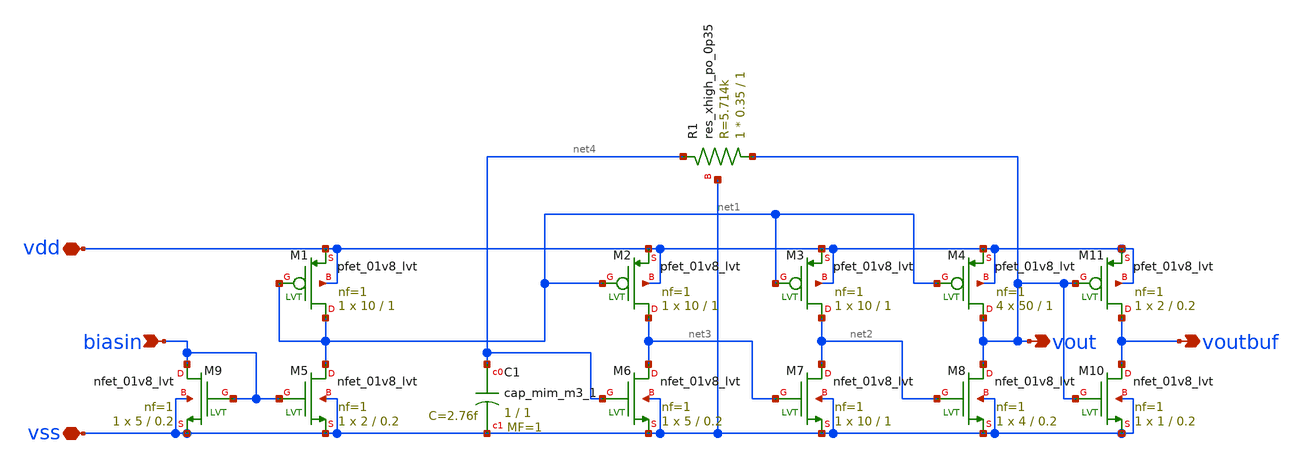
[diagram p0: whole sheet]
** sch_path: Circuits/lowpowersystem1/xschem/lphysteresistoscillatorsym5.sch
**.subckt lphysteresistoscillatorsym5 biasin vss vdd voutbuf vout
*.ipin biasin
*.iopin vss
*.iopin vdd
*.opin voutbuf
*.opin vout
XM1 net1 net1 vdd vdd sky130_fd_pr__pfet_01v8_lvt L=1 W=10 nf=1 ad='int((nf+1)/2) * W/nf * 0.29' as='int((nf+2)/2) * W/nf * 0.29'
+ pd='2*int((nf+1)/2) * (W/nf + 0.29)' ps='2*int((nf+2)/2) * (W/nf + 0.29)' nrd='0.29 / W' nrs='0.29 / W'
+ sa=0 sb=0 sd=0 mult=1 m=1
XM2 net3 net1 vdd vdd sky130_fd_pr__pfet_01v8_lvt L=1 W=10 nf=1 ad='int((nf+1)/2) * W/nf * 0.29' as='int((nf+2)/2) * W/nf * 0.29'
+ pd='2*int((nf+1)/2) * (W/nf + 0.29)' ps='2*int((nf+2)/2) * (W/nf + 0.29)' nrd='0.29 / W' nrs='0.29 / W'
+ sa=0 sb=0 sd=0 mult=1 m=1
XM3 net2 net1 vdd vdd sky130_fd_pr__pfet_01v8_lvt L=1 W=10 nf=1 ad='int((nf+1)/2) * W/nf * 0.29' as='int((nf+2)/2) * W/nf * 0.29'
+ pd='2*int((nf+1)/2) * (W/nf + 0.29)' ps='2*int((nf+2)/2) * (W/nf + 0.29)' nrd='0.29 / W' nrs='0.29 / W'
+ sa=0 sb=0 sd=0 mult=1 m=1
XM4 vout net1 vdd vdd sky130_fd_pr__pfet_01v8_lvt L=1 W=50 nf=1 ad='int((nf+1)/2) * W/nf * 0.29' as='int((nf+2)/2) * W/nf * 0.29'
+ pd='2*int((nf+1)/2) * (W/nf + 0.29)' ps='2*int((nf+2)/2) * (W/nf + 0.29)' nrd='0.29 / W' nrs='0.29 / W'
+ sa=0 sb=0 sd=0 mult=4 m=4
XM5 net1 biasin vss vss sky130_fd_pr__nfet_01v8_lvt L=0.2 W=2 nf=1 ad='int((nf+1)/2) * W/nf * 0.29' as='int((nf+2)/2) * W/nf * 0.29'
+ pd='2*int((nf+1)/2) * (W/nf + 0.29)' ps='2*int((nf+2)/2) * (W/nf + 0.29)' nrd='0.29 / W' nrs='0.29 / W'
+ sa=0 sb=0 sd=0 mult=1 m=1
XM6 net3 net4 vss vss sky130_fd_pr__nfet_01v8_lvt L=0.2 W=5 nf=1 ad='int((nf+1)/2) * W/nf * 0.29' as='int((nf+2)/2) * W/nf * 0.29'
+ pd='2*int((nf+1)/2) * (W/nf + 0.29)' ps='2*int((nf+2)/2) * (W/nf + 0.29)' nrd='0.29 / W' nrs='0.29 / W'
+ sa=0 sb=0 sd=0 mult=1 m=1
XM7 net2 net3 vss vss sky130_fd_pr__nfet_01v8_lvt L=1 W=10 nf=1 ad='int((nf+1)/2) * W/nf * 0.29' as='int((nf+2)/2) * W/nf * 0.29'
+ pd='2*int((nf+1)/2) * (W/nf + 0.29)' ps='2*int((nf+2)/2) * (W/nf + 0.29)' nrd='0.29 / W' nrs='0.29 / W'
+ sa=0 sb=0 sd=0 mult=1 m=1
XM8 vout net2 vss vss sky130_fd_pr__nfet_01v8_lvt L=0.2 W=4 nf=1 ad='int((nf+1)/2) * W/nf * 0.29' as='int((nf+2)/2) * W/nf * 0.29'
+ pd='2*int((nf+1)/2) * (W/nf + 0.29)' ps='2*int((nf+2)/2) * (W/nf + 0.29)' nrd='0.29 / W' nrs='0.29 / W'
+ sa=0 sb=0 sd=0 mult=1 m=1
XM9 biasin biasin vss vss sky130_fd_pr__nfet_01v8_lvt L=0.2 W=5 nf=1 ad='int((nf+1)/2) * W/nf * 0.29'
+ as='int((nf+2)/2) * W/nf * 0.29' pd='2*int((nf+1)/2) * (W/nf + 0.29)' ps='2*int((nf+2)/2) * (W/nf + 0.29)'
+ nrd='0.29 / W' nrs='0.29 / W' sa=0 sb=0 sd=0 mult=1 m=1
XM10 voutbuf vout vss vss sky130_fd_pr__nfet_01v8_lvt L=0.2 W=1 nf=1 ad='int((nf+1)/2) * W/nf * 0.29'
+ as='int((nf+2)/2) * W/nf * 0.29' pd='2*int((nf+1)/2) * (W/nf + 0.29)' ps='2*int((nf+2)/2) * (W/nf + 0.29)'
+ nrd='0.29 / W' nrs='0.29 / W' sa=0 sb=0 sd=0 mult=1 m=1
XM11 voutbuf vout vdd vdd sky130_fd_pr__pfet_01v8_lvt L=0.2 W=2 nf=1 ad='int((nf+1)/2) * W/nf * 0.29'
+ as='int((nf+2)/2) * W/nf * 0.29' pd='2*int((nf+1)/2) * (W/nf + 0.29)' ps='2*int((nf+2)/2) * (W/nf + 0.29)'
+ nrd='0.29 / W' nrs='0.29 / W' sa=0 sb=0 sd=0 mult=1 m=1
XC1 net4 vss sky130_fd_pr__cap_mim_m3_1 W=1 L=1 MF=1 m=1
XR1 vout net4 vss sky130_fd_pr__res_xhigh_po_0p35 L=1 mult=1 m=1
**.ends
.end
